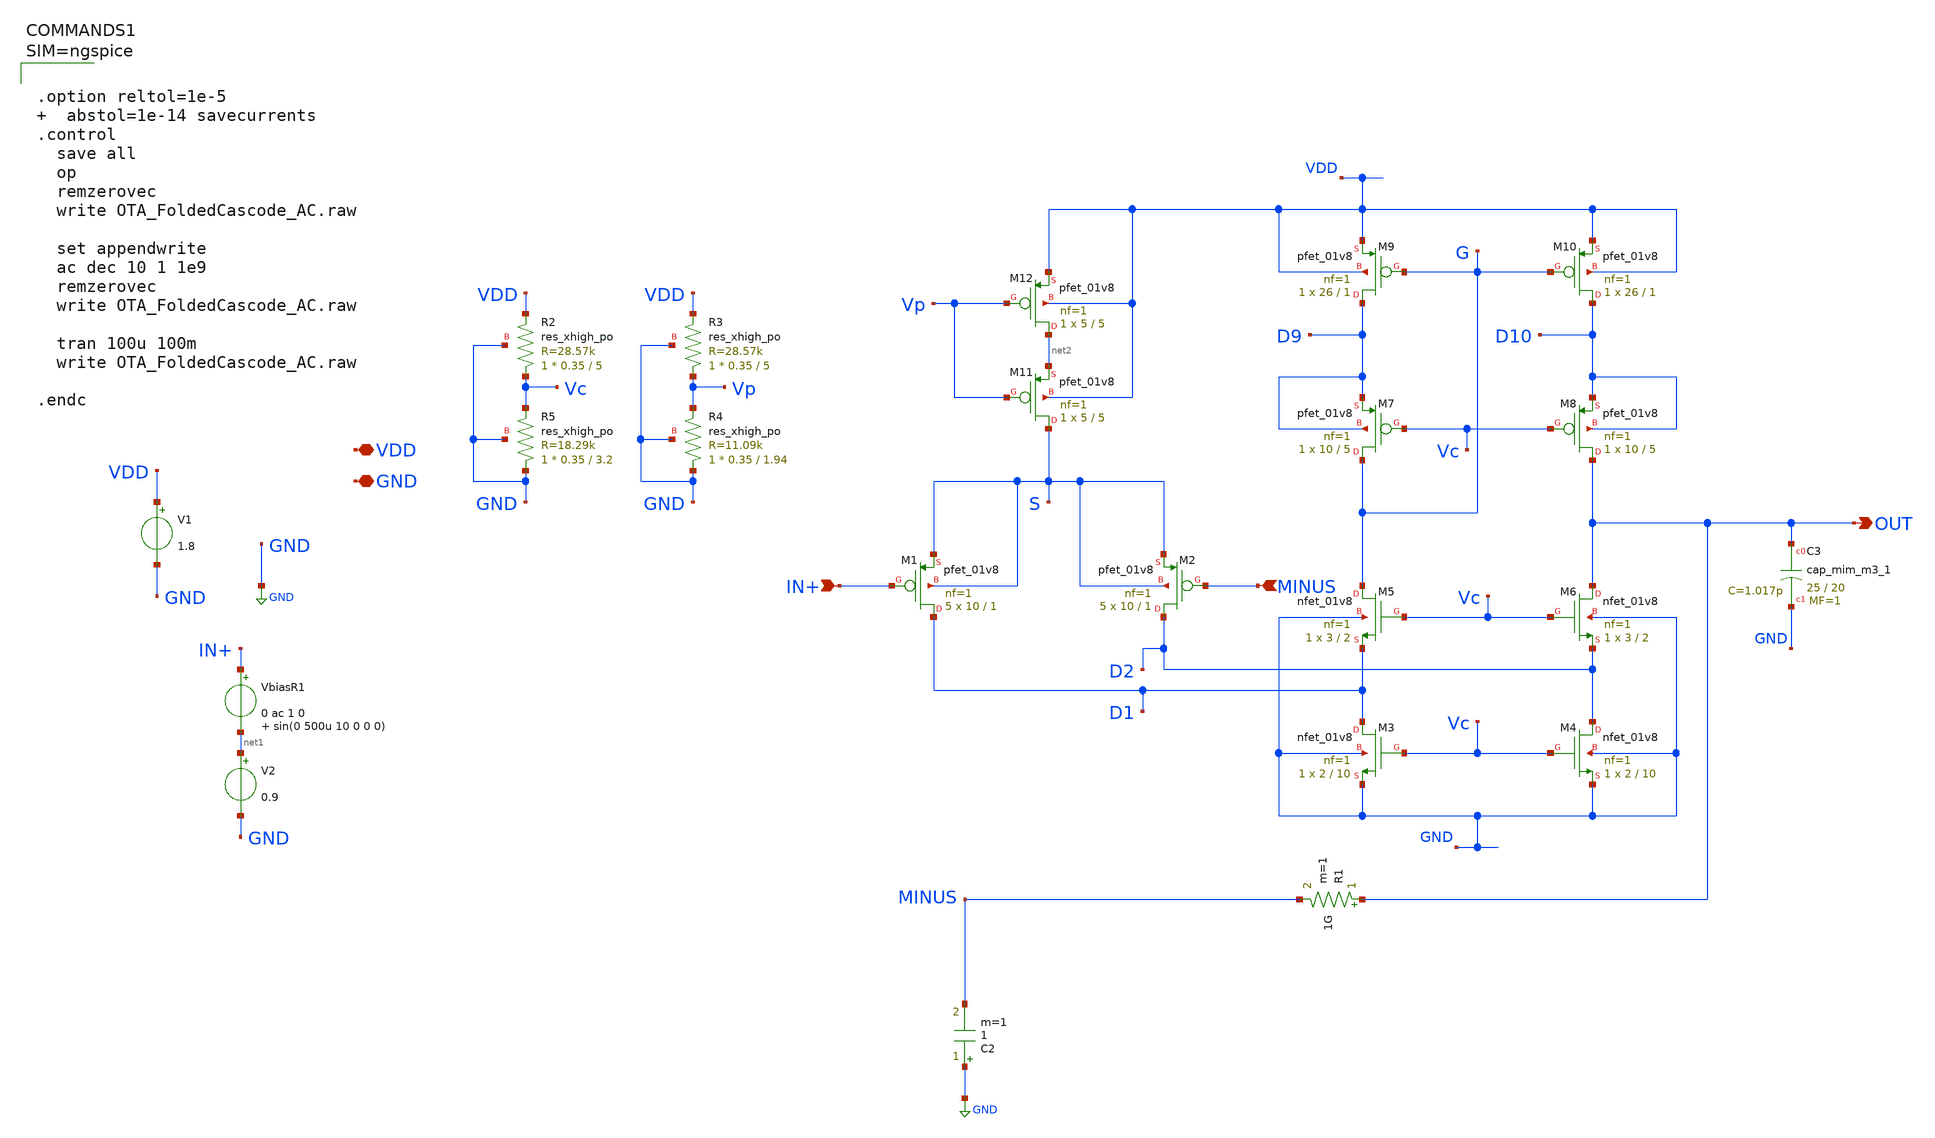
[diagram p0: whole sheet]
** sch_path: xschem/OTA_FoldedCascode_AC.sch
**.subckt OTA_FoldedCascode_AC VDD GND OUT IN+ MINUS
*.iopin VDD
*.iopin GND
*.opin OUT
*.ipin IN+
*.ipin MINUS
VbiasR1 IN+ net1 0 ac 1 0 sin(0 500u 10 0 0 0)
V2 net1 GND 0.9
V1 VDD GND 1.8
XC3 OUT GND sky130_fd_pr__cap_mim_m3_1 W=25 L=20 MF=1 m=1
C2 GND MINUS 1 m=1
R1 OUT MINUS 1G m=1
XM1 D1 IN+ S S sky130_fd_pr__pfet_01v8 L=1 W=10 nf=1 ad='int((nf+1)/2) * W/nf * 0.29' as='int((nf+2)/2) * W/nf * 0.29'
+ pd='2*int((nf+1)/2) * (W/nf + 0.29)' ps='2*int((nf+2)/2) * (W/nf + 0.29)' nrd='0.29 / W' nrs='0.29 / W'
+ sa=0 sb=0 sd=0 mult=5 m=5
XM2 D2 MINUS S S sky130_fd_pr__pfet_01v8 L=1 W=10 nf=1 ad='int((nf+1)/2) * W/nf * 0.29' as='int((nf+2)/2) * W/nf * 0.29'
+ pd='2*int((nf+1)/2) * (W/nf + 0.29)' ps='2*int((nf+2)/2) * (W/nf + 0.29)' nrd='0.29 / W' nrs='0.29 / W'
+ sa=0 sb=0 sd=0 mult=5 m=5
XM3 D1 Vc GND GND sky130_fd_pr__nfet_01v8 L=10 W=2 nf=1 ad='int((nf+1)/2) * W/nf * 0.29' as='int((nf+2)/2) * W/nf * 0.29'
+ pd='2*int((nf+1)/2) * (W/nf + 0.29)' ps='2*int((nf+2)/2) * (W/nf + 0.29)' nrd='0.29 / W' nrs='0.29 / W'
+ sa=0 sb=0 sd=0 mult=1 m=1
XM4 D2 Vc GND GND sky130_fd_pr__nfet_01v8 L=10 W=2 nf=1 ad='int((nf+1)/2) * W/nf * 0.29' as='int((nf+2)/2) * W/nf * 0.29'
+ pd='2*int((nf+1)/2) * (W/nf + 0.29)' ps='2*int((nf+2)/2) * (W/nf + 0.29)' nrd='0.29 / W' nrs='0.29 / W'
+ sa=0 sb=0 sd=0 mult=1 m=1
XM5 G Vc D1 GND sky130_fd_pr__nfet_01v8 L=2 W=3 nf=1 ad='int((nf+1)/2) * W/nf * 0.29' as='int((nf+2)/2) * W/nf * 0.29'
+ pd='2*int((nf+1)/2) * (W/nf + 0.29)' ps='2*int((nf+2)/2) * (W/nf + 0.29)' nrd='0.29 / W' nrs='0.29 / W'
+ sa=0 sb=0 sd=0 mult=1 m=1
XM6 OUT Vc D2 GND sky130_fd_pr__nfet_01v8 L=2 W=3 nf=1 ad='int((nf+1)/2) * W/nf * 0.29' as='int((nf+2)/2) * W/nf * 0.29'
+ pd='2*int((nf+1)/2) * (W/nf + 0.29)' ps='2*int((nf+2)/2) * (W/nf + 0.29)' nrd='0.29 / W' nrs='0.29 / W'
+ sa=0 sb=0 sd=0 mult=1 m=1
XM7 G Vc D9 D9 sky130_fd_pr__pfet_01v8 L=5 W=10 nf=1 ad='int((nf+1)/2) * W/nf * 0.29' as='int((nf+2)/2) * W/nf * 0.29'
+ pd='2*int((nf+1)/2) * (W/nf + 0.29)' ps='2*int((nf+2)/2) * (W/nf + 0.29)' nrd='0.29 / W' nrs='0.29 / W'
+ sa=0 sb=0 sd=0 mult=1 m=1
XM8 OUT Vc D10 D10 sky130_fd_pr__pfet_01v8 L=5 W=10 nf=1 ad='int((nf+1)/2) * W/nf * 0.29' as='int((nf+2)/2) * W/nf * 0.29'
+ pd='2*int((nf+1)/2) * (W/nf + 0.29)' ps='2*int((nf+2)/2) * (W/nf + 0.29)' nrd='0.29 / W' nrs='0.29 / W'
+ sa=0 sb=0 sd=0 mult=1 m=1
XM9 D9 G VDD VDD sky130_fd_pr__pfet_01v8 L=1 W=26 nf=1 ad='int((nf+1)/2) * W/nf * 0.29' as='int((nf+2)/2) * W/nf * 0.29'
+ pd='2*int((nf+1)/2) * (W/nf + 0.29)' ps='2*int((nf+2)/2) * (W/nf + 0.29)' nrd='0.29 / W' nrs='0.29 / W'
+ sa=0 sb=0 sd=0 mult=1 m=1
XM10 D10 G VDD VDD sky130_fd_pr__pfet_01v8 L=1 W=26 nf=1 ad='int((nf+1)/2) * W/nf * 0.29' as='int((nf+2)/2) * W/nf * 0.29'
+ pd='2*int((nf+1)/2) * (W/nf + 0.29)' ps='2*int((nf+2)/2) * (W/nf + 0.29)' nrd='0.29 / W' nrs='0.29 / W'
+ sa=0 sb=0 sd=0 mult=1 m=1
XM11 S Vp net2 VDD sky130_fd_pr__pfet_01v8 L=5 W=5 nf=1 ad='int((nf+1)/2) * W/nf * 0.29' as='int((nf+2)/2) * W/nf * 0.29'
+ pd='2*int((nf+1)/2) * (W/nf + 0.29)' ps='2*int((nf+2)/2) * (W/nf + 0.29)' nrd='0.29 / W' nrs='0.29 / W'
+ sa=0 sb=0 sd=0 mult=1 m=1
XM12 net2 Vp VDD VDD sky130_fd_pr__pfet_01v8 L=5 W=5 nf=1 ad='int((nf+1)/2) * W/nf * 0.29' as='int((nf+2)/2) * W/nf * 0.29'
+ pd='2*int((nf+1)/2) * (W/nf + 0.29)' ps='2*int((nf+2)/2) * (W/nf + 0.29)' nrd='0.29 / W' nrs='0.29 / W'
+ sa=0 sb=0 sd=0 mult=1 m=1
XR5 GND Vc GND sky130_fd_pr__res_xhigh_po W=0.35 L=3.2 mult=1 m=1
XR2 Vc VDD GND sky130_fd_pr__res_xhigh_po W=0.35 L=5 mult=1 m=1
XR3 Vp VDD GND sky130_fd_pr__res_xhigh_po W=0.35 L=5 mult=1 m=1
XR4 GND Vp GND sky130_fd_pr__res_xhigh_po W=0.35 L=1.94 mult=1 m=1
**** begin user architecture code



.option reltol=1e-5   abstol=1e-14 savecurrents
.control
  save all
  op
  remzerovec
  write OTA_FoldedCascode_AC.raw

  set appendwrite
  ac dec 10 1 1e9
  remzerovec
  write OTA_FoldedCascode_AC.raw

  tran 100u 100m
  write OTA_FoldedCascode_AC.raw

.endc



.lib $::SKYWATER_MODELS/sky130.lib.spice tt
**** end user architecture code
**.ends
.GLOBAL GND
.end
